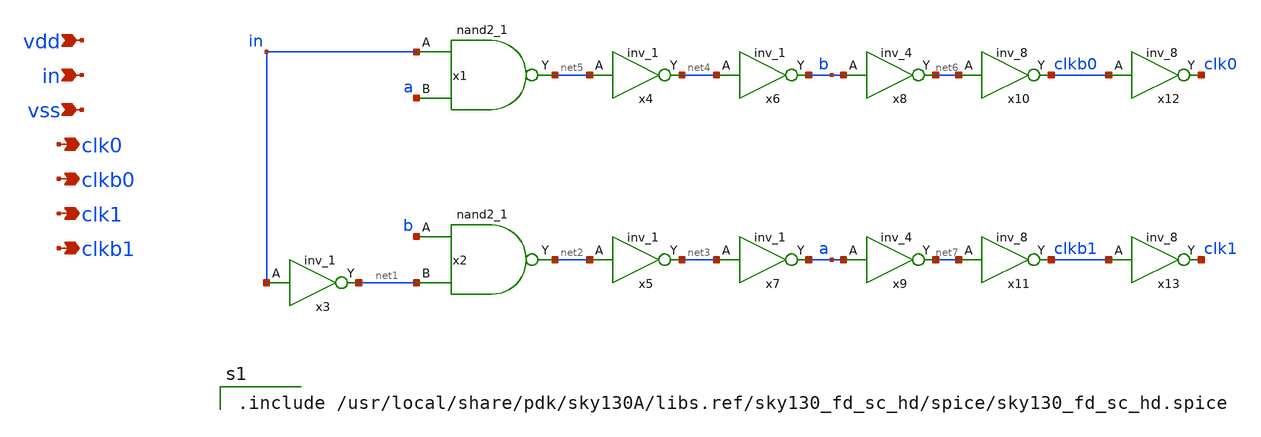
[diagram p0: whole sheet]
** sch_path: xschem/nooverlap_clk.sch
**.subckt nooverlap_clk vdd in vss clk0 clkb0 clk1 clkb1
*.ipin vdd
*.ipin in
*.ipin vss
*.opin clk0
*.opin clkb0
*.opin clk1
*.opin clkb1
x1 in a vss vss vdd vdd net5 sky130_fd_sc_hd__nand2_1
x2 b net1 vss vss vdd vdd net2 sky130_fd_sc_hd__nand2_1
x3 in vss vss vdd vdd net1 sky130_fd_sc_hd__inv_1
x4 net5 vss vss vdd vdd net4 sky130_fd_sc_hd__inv_1
x5 net2 vss vss vdd vdd net3 sky130_fd_sc_hd__inv_1
x6 net4 vss vss vdd vdd b sky130_fd_sc_hd__inv_1
x7 net3 vss vss vdd vdd a sky130_fd_sc_hd__inv_1
x8 b vss vss vdd vdd net6 sky130_fd_sc_hd__inv_4
x9 a vss vss vdd vdd net7 sky130_fd_sc_hd__inv_4
x10 net6 vss vss vdd vdd clkb0 sky130_fd_sc_hd__inv_8
x11 net7 vss vss vdd vdd clkb1 sky130_fd_sc_hd__inv_8
x12 clkb0 vss vss vdd vdd clk0 sky130_fd_sc_hd__inv_8
x13 clkb1 vss vss vdd vdd clk1 sky130_fd_sc_hd__inv_8
**** begin user architecture code

.include /usr/local/share/pdk/sky130A/libs.ref/sky130_fd_sc_hd/spice/sky130_fd_sc_hd.spice

**** end user architecture code
**.ends
.end
